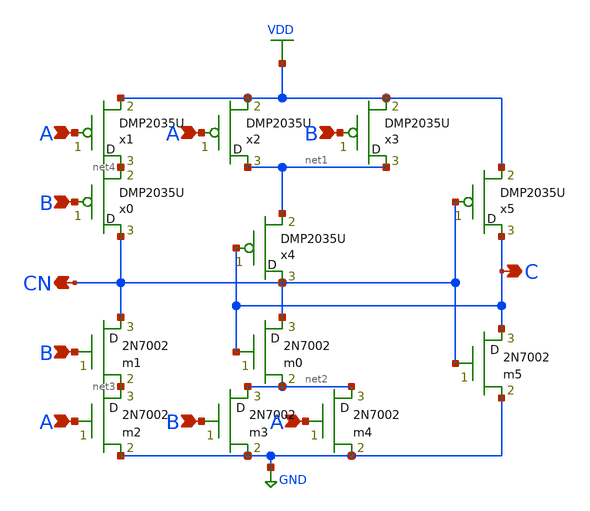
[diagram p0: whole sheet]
** sch_path: cells/xschem/ASYNC1.sch
**.subckt ASYNC1 A B A B C CN B A B A
*.ipin A
*.ipin B
*.ipin A
*.ipin B
*.opin C
*.opin CN
*.ipin B
*.ipin A
*.ipin B
*.ipin A
m1 CN B net3 enbsim3 m=1
x1 net4 A VDD epbsim3 m=1
x0 CN B net4 epbsim3 m=1
x2 net1 A VDD epbsim3 m=1
x3 net1 B VDD epbsim3 m=1
x4 CN C net1 epbsim3 m=1
x5 C CN VDD epbsim3 m=1
m0 CN C net2 enbsim3 m=1
m2 net3 A GND enbsim3 m=1
m3 net2 B GND enbsim3 m=1
m4 net2 A GND enbsim3 m=1
m5 C CN GND enbsim3 m=1
**.ends
.GLOBAL GND
.GLOBAL VDD
.end
